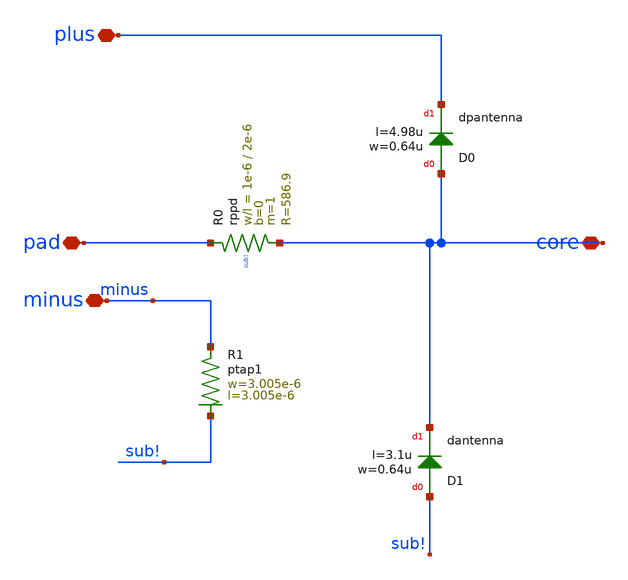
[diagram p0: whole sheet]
** sch_path: ihp-sg13g2/libs.ref/sg13g2_io/sch/xschem/sg13g2_SecondaryProtection.sch
**.subckt sg13g2_SecondaryProtection core pad plus minus
*.iopin core
*.iopin pad
*.iopin plus
*.iopin minus
XD0 core plus dpantenna l=4.98u w=0.64u
XD1 sub! core dantenna l=3.1u w=0.64u
XR0 pad core sub! rppd w=1e-6 l=2e-6 m=1 b=0 mm_ok=1
XR1 minus sub! ptap1 R=46.56 w=3.005e-6 l=3.005e-6
**.ends
.end
